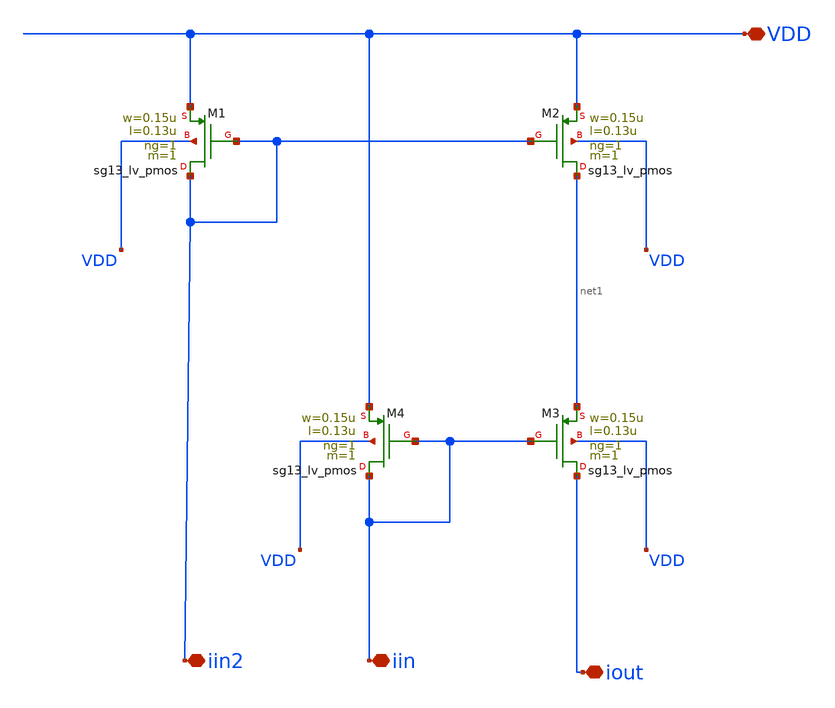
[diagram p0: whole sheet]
** sch_path: analog-db/templates/current_mirror/pmos_current_source/high_swing_cascode_current_mirror.sch
* Copyright 2026 MacAnalog Research Group
**.subckt high_swing_cascode_current_mirror iout iin VDD iin2
*.iopin iout
*.iopin iin
*.iopin VDD
*.iopin iin2
XM1 iin2 iin2 VDD VDD sg13_lv_pmos w=0.15u l=0.13u ng=1 m=1 mm_ok=1
XM2 net1 iin2 VDD VDD sg13_lv_pmos w=0.15u l=0.13u ng=1 m=1 mm_ok=1
XM3 iout iin net1 VDD sg13_lv_pmos w=0.15u l=0.13u ng=1 m=1 mm_ok=1
XM4 iin iin VDD VDD sg13_lv_pmos w=0.15u l=0.13u ng=1 m=1 mm_ok=1
**.ends
.end
